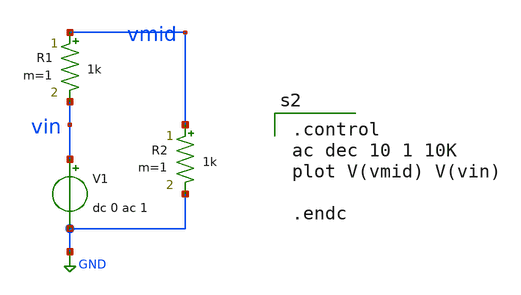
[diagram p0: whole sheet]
** sch_path: xschem/untitled.sch
**.subckt untitled
V1 vin GND dc 0 ac 1
R1 vmid vin 1k m=1
R2 vmid GND 1k m=1
**** begin user architecture code
.lib $::SKYWATER_MODELS/sky130.lib.spice tt
.include $::PDKPATH/libs.ref/sky130_fd_sc_hvl/spice/sky130_fd_sc_hvl.spice

.control
ac dec 10 1 10K
plot V(vmid) V(vin)

.endc


**** end user architecture code
**.ends
.GLOBAL GND
.end
